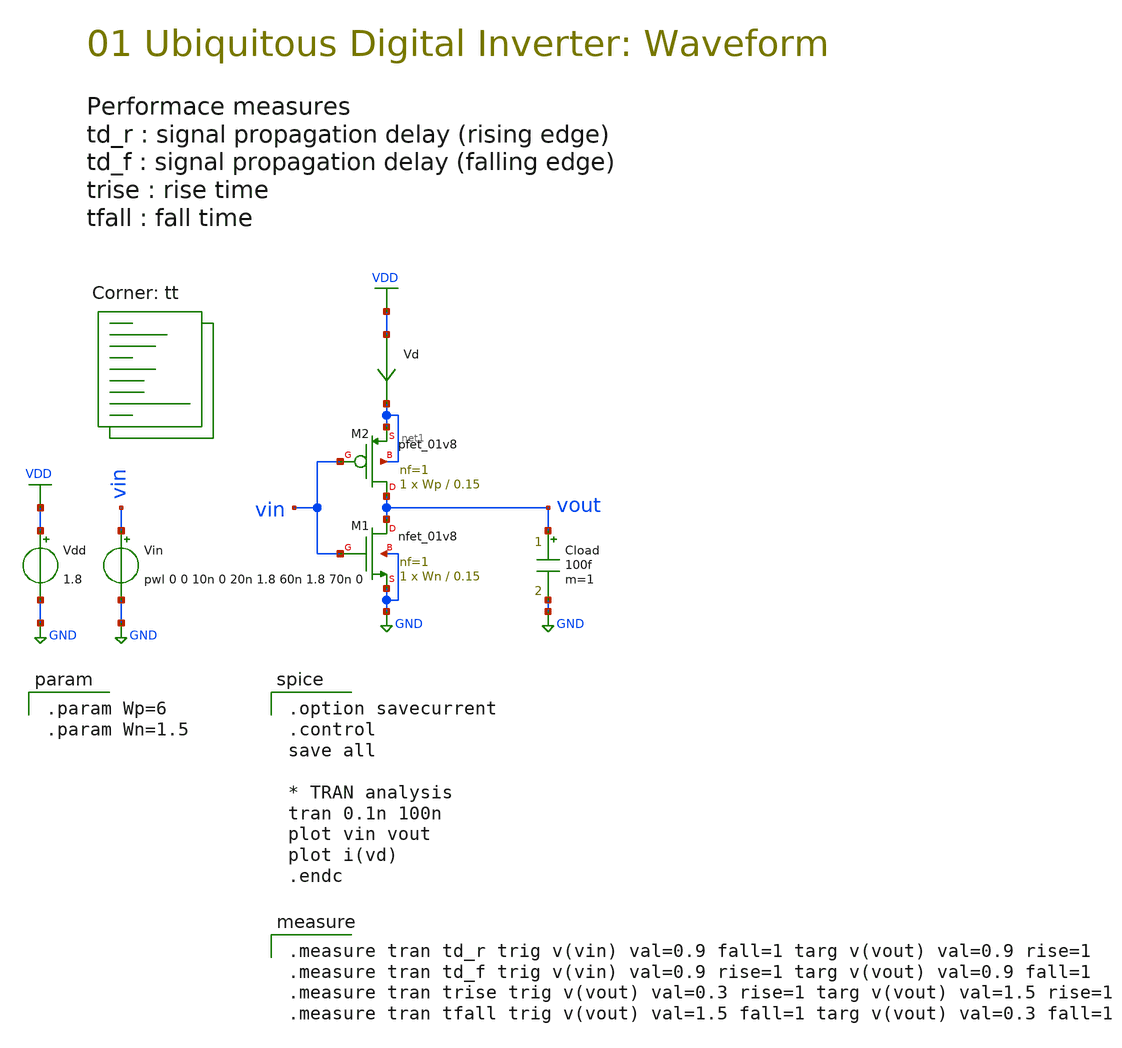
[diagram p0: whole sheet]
** sch_path: 01-b_inverter_tran.sch
**.subckt 01-b_inverter_tran
Vdd VDD GND 1.8
Vin vin GND pwl 0 0 10n 0 20n 1.8 60n 1.8 70n 0
Cload vout GND 100f m=1
XM2 vout vin net1 net1 sky130_fd_pr__pfet_01v8 L=0.15 W=Wp nf=1 ad='int((nf+1)/2) * W/nf * 0.29' as='int((nf+2)/2) * W/nf * 0.29'
+ pd='2*int((nf+1)/2) * (W/nf + 0.29)' ps='2*int((nf+2)/2) * (W/nf + 0.29)' nrd='0.29 / W' nrs='0.29 / W'
+ sa=0 sb=0 sd=0 mult=1 m=1
XM1 vout vin GND GND sky130_fd_pr__nfet_01v8 L=0.15 W=Wn nf=1 ad='int((1 + 1)/2) * Wn / 1 * 0.29' as='int((1 + 2)/2) * Wn / 1 * 0.29'
+ pd='2*int((1 + 1)/2) * (Wn / 1 + 0.29)' ps='2*int((1 + 2)/2) * (Wn / 1 + 0.29)' nrd='0.29 / Wn ' nrs='0.29 / Wn '
+ sa=0 sb=0 sd=0 mult=1 m=1
Vd VDD net1 0
.save i(vd)
**** begin user architecture code
.lib $::SKYWATER_MODELS/sky130.lib.spice tt

.param Wp=6
.param Wn=1.5


.option savecurrent
.control
save all

* TRAN analysis
tran 0.1n 100n
plot vin vout
plot i(vd)
.endc


.measure tran td_r trig v(vin) val=0.9 fall=1 targ v(vout) val=0.9 rise=1
.measure tran td_f trig v(vin) val=0.9 rise=1 targ v(vout) val=0.9 fall=1
.measure tran trise trig v(vout) val=0.3 rise=1 targ v(vout) val=1.5 rise=1
.measure tran tfall trig v(vout) val=1.5 fall=1 targ v(vout) val=0.3 fall=1

**** end user architecture code
**.ends
.GLOBAL GND
.GLOBAL VDD
.end
